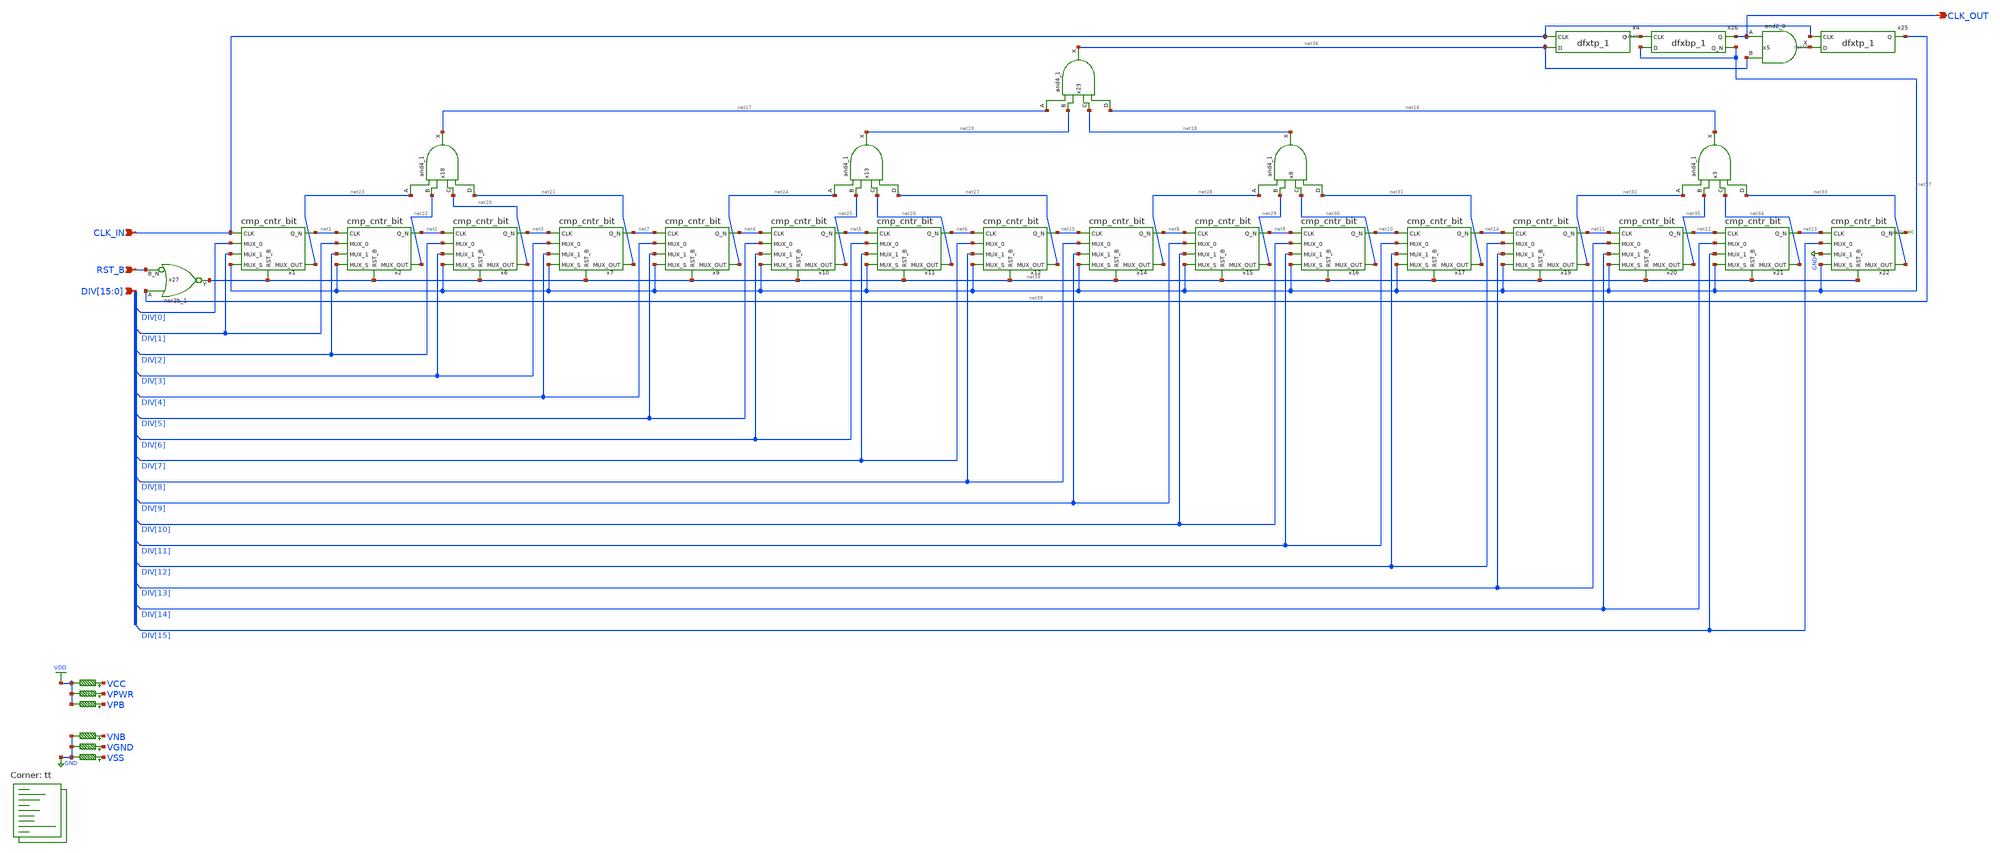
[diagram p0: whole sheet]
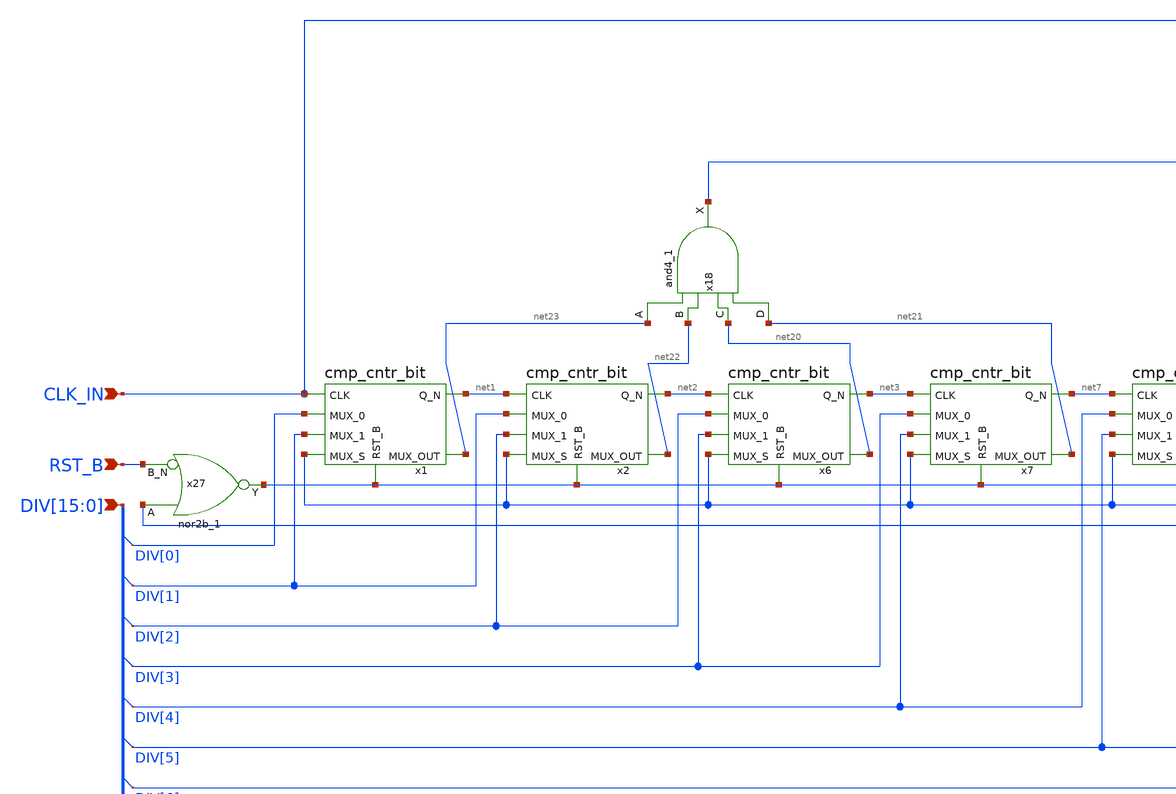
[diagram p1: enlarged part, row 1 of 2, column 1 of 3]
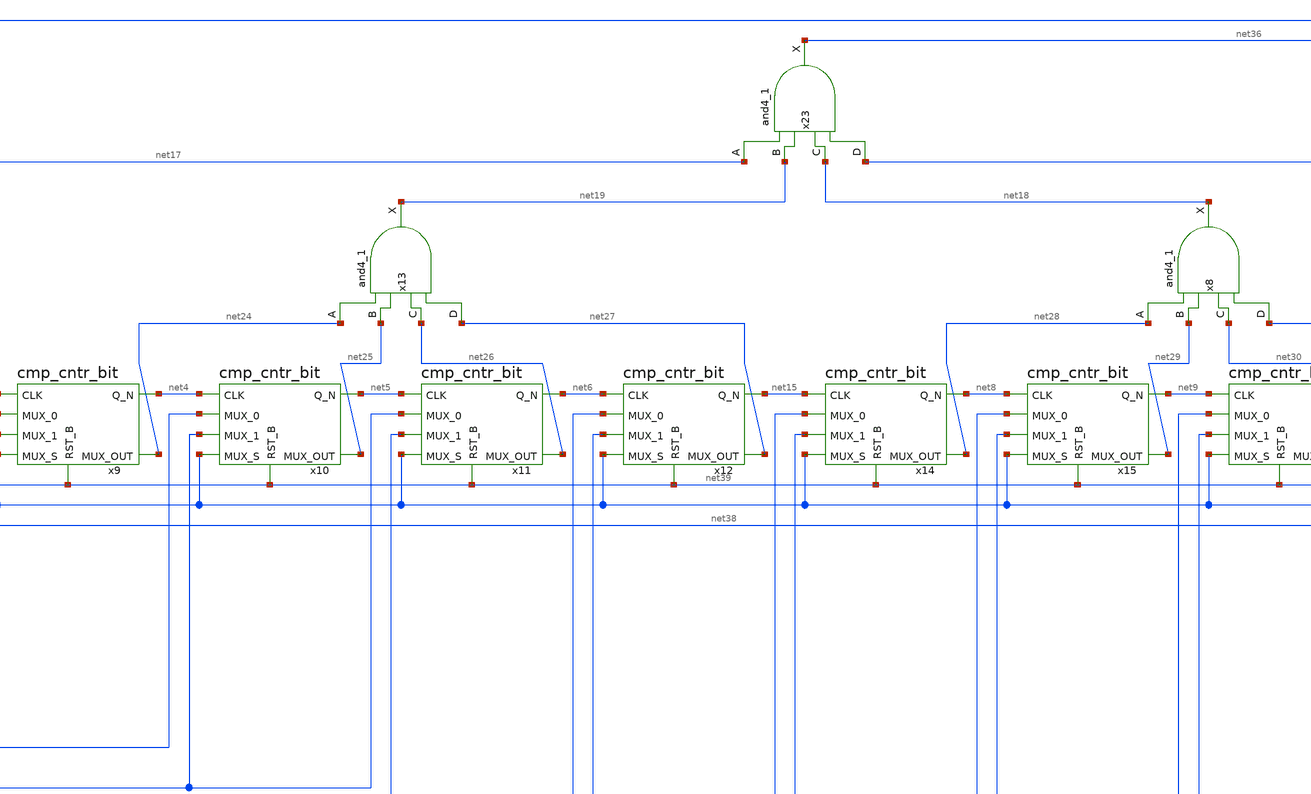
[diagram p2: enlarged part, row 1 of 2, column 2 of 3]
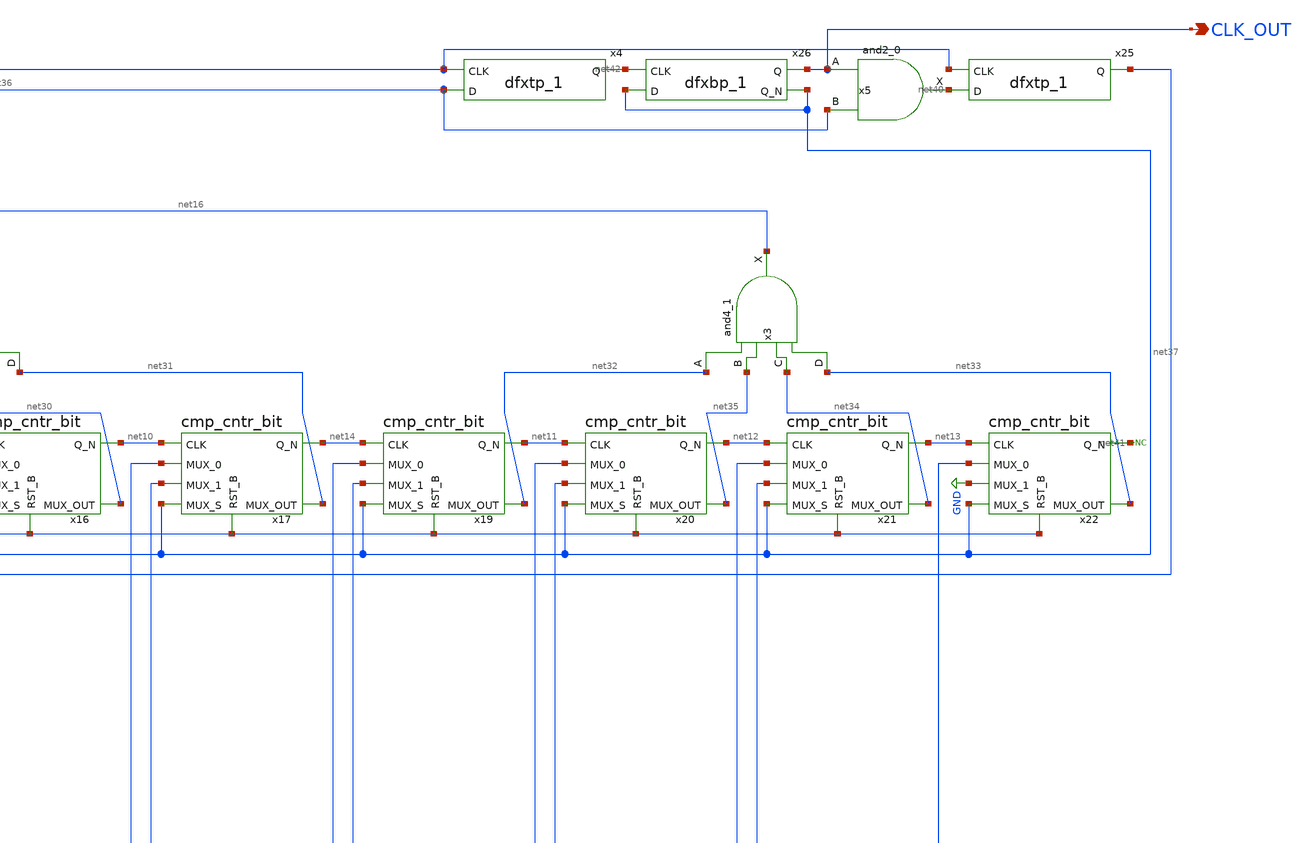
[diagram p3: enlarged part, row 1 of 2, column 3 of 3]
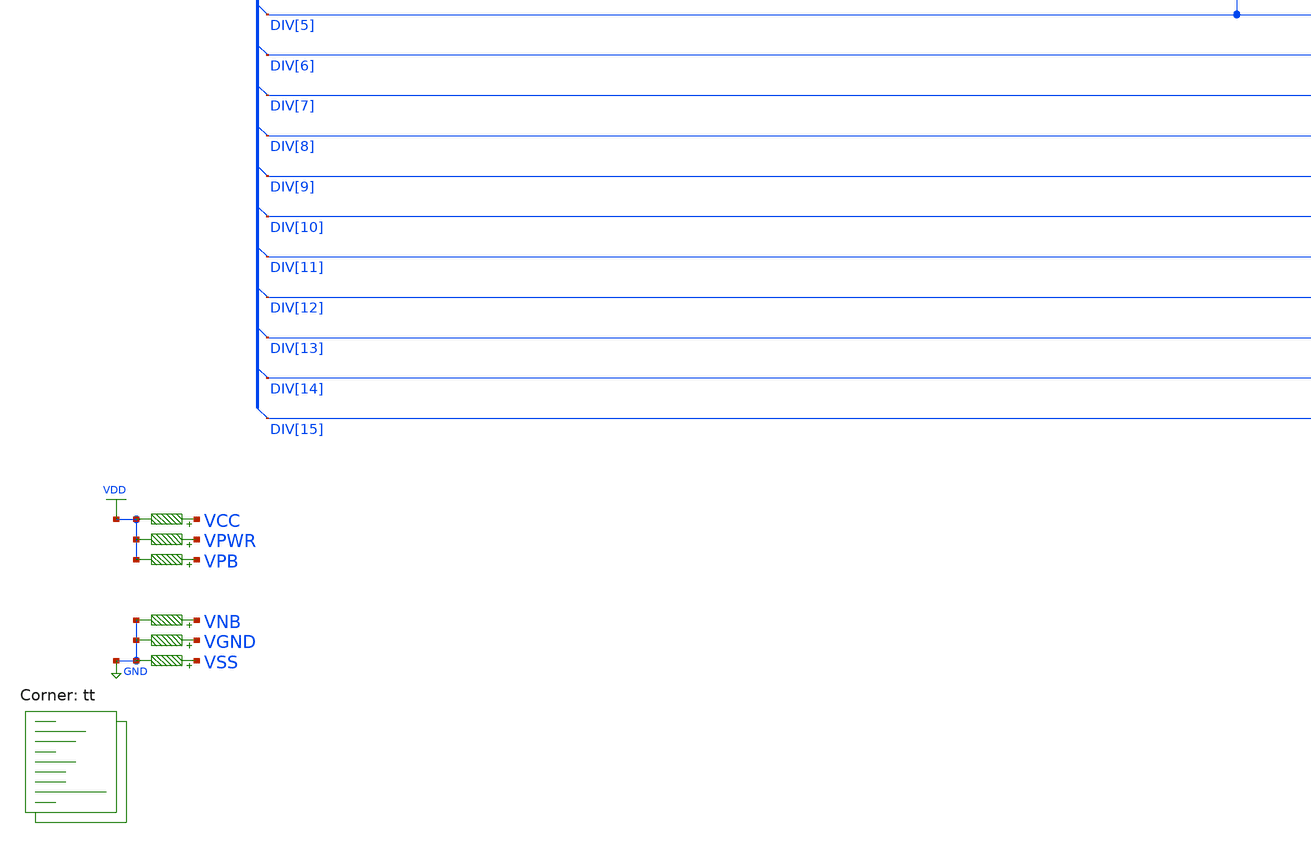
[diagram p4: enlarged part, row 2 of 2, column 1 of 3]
** sch_path: int_div.sch
**.subckt int_div CLK_OUT CLK_IN RST_B
*+ DIV[15],DIV[14],DIV[13],DIV[12],DIV[11],DIV[10],DIV[9],DIV[8],DIV[7],DIV[6],DIV[5],DIV[4],DIV[3],DIV[2],DIV[1],DIV[0]
*.opin CLK_OUT
*.ipin CLK_IN
*.ipin RST_B
*.ipin
*+ DIV[15],DIV[14],DIV[13],DIV[12],DIV[11],DIV[10],DIV[9],DIV[8],DIV[7],DIV[6],DIV[5],DIV[4],DIV[3],DIV[2],DIV[1],DIV[0]
R1 VNB GND 0.01 m=1
R2 VPB VDD 0.01 m=1
R3 VPWR VDD 0.01 m=1
R4 VGND GND 0.01 m=1
R5 VSS GND 0.01 m=1
R6 VCC VDD 0.01 m=1
x3 net32 net35 net34 net33 VGND VNB VPB VPWR net16 sky130_fd_sc_hd__and4_1
x5 CLK_OUT net36 VGND VNB VPB VPWR net40 sky130_fd_sc_hd__and2_0
x1 net23 CLK_IN net1 net39 DIV[0] DIV[1] net37 cmp_cntr_bit
x2 net22 net1 net2 net39 DIV[1] DIV[2] net37 cmp_cntr_bit
x6 net20 net2 net3 net39 DIV[2] DIV[3] net37 cmp_cntr_bit
x7 net21 net3 net7 net39 DIV[3] DIV[4] net37 cmp_cntr_bit
x8 net28 net29 net30 net31 VGND VNB VPB VPWR net18 sky130_fd_sc_hd__and4_1
x9 net24 net7 net4 net39 DIV[4] DIV[5] net37 cmp_cntr_bit
x10 net25 net4 net5 net39 DIV[5] DIV[6] net37 cmp_cntr_bit
x11 net26 net5 net6 net39 DIV[6] DIV[7] net37 cmp_cntr_bit
x12 net27 net6 net15 net39 DIV[7] DIV[8] net37 cmp_cntr_bit
x13 net24 net25 net26 net27 VGND VNB VPB VPWR net19 sky130_fd_sc_hd__and4_1
x14 net28 net15 net8 net39 DIV[8] DIV[9] net37 cmp_cntr_bit
x15 net29 net8 net9 net39 DIV[9] DIV[10] net37 cmp_cntr_bit
x16 net30 net9 net10 net39 DIV[10] DIV[11] net37 cmp_cntr_bit
x17 net31 net10 net14 net39 DIV[11] DIV[12] net37 cmp_cntr_bit
x18 net23 net22 net20 net21 VGND VNB VPB VPWR net17 sky130_fd_sc_hd__and4_1
x19 net32 net14 net11 net39 DIV[12] DIV[13] net37 cmp_cntr_bit
x20 net35 net11 net12 net39 DIV[13] DIV[14] net37 cmp_cntr_bit
x21 net34 net12 net13 net39 DIV[14] DIV[15] net37 cmp_cntr_bit
x22 net33 net13 net41 net39 DIV[15] GND net37 cmp_cntr_bit
x23 net17 net19 net18 net16 VGND VNB VPB VPWR net36 sky130_fd_sc_hd__and4_1
x4 CLK_IN net36 VGND VNB VPB VPWR net42 sky130_fd_sc_hd__dfxtp_1
x25 CLK_IN net40 VGND VNB VPB VPWR net38 sky130_fd_sc_hd__dfxtp_1
x26 net42 net37 VGND VNB VPB VPWR CLK_OUT net37 sky130_fd_sc_hd__dfxbp_1
* noconn #net41
x27 net38 RST_B VGND VNB VPB VPWR net39 sky130_fd_sc_hd__nor2b_1
**** begin user architecture code
.lib $::SKYWATER_MODELS/sky130.lib.spice tt


.include /usr/local/share/pdk/sky130A/libs.ref/sky130_fd_sc_hd/spice/sky130_fd_sc_hd.spice tt
.control
  save all
  tran .1n 10u
  write top.raw
  quit 0
.endc


**** end user architecture code
**.ends
.GLOBAL GND
.GLOBAL VDD
.end
